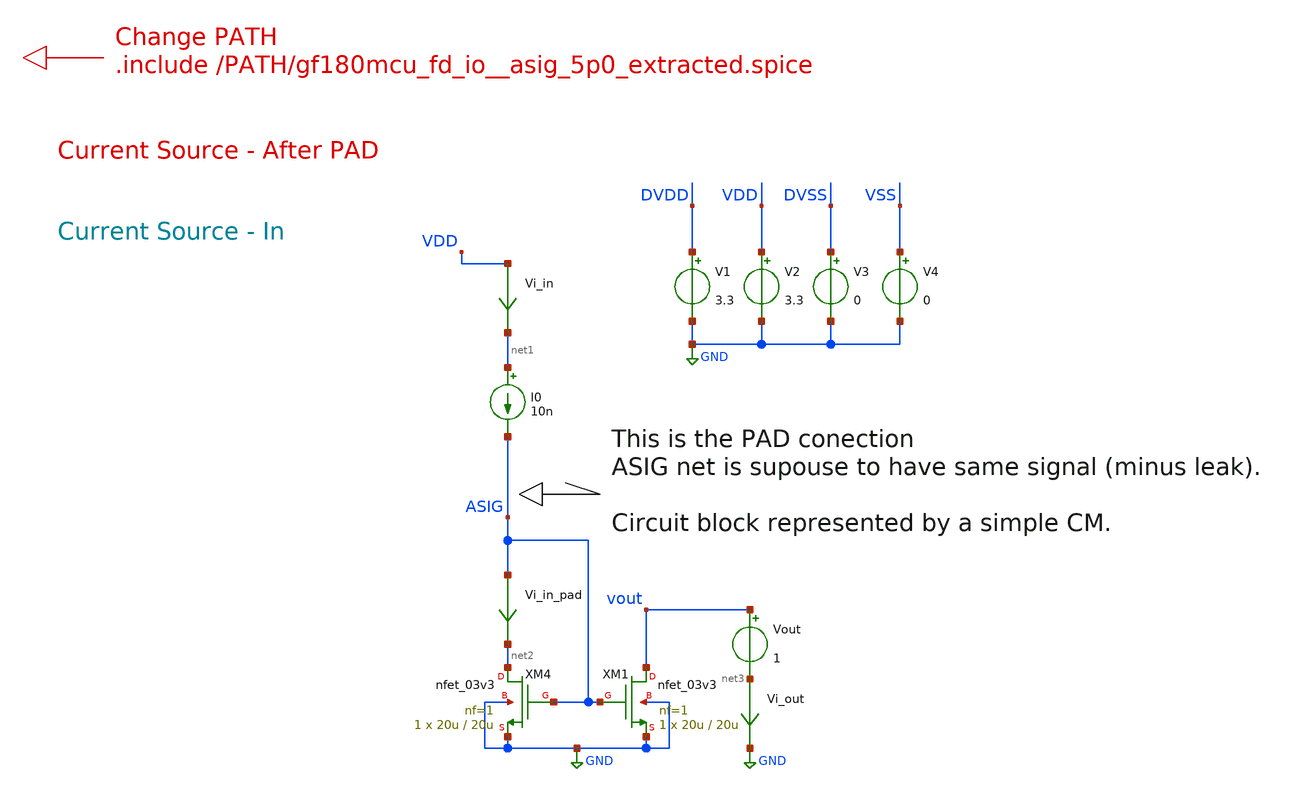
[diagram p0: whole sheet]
** sch_path: designs/Chipathon2025_pads/xschem/analog_leak_pads.sch
**.subckt analog_leak_pads
V1 DVDD GND 3.3
V2 VDD GND 3.3
V3 DVSS GND 0
V4 VSS GND 0
XM1 vout ASIG GND GND nfet_03v3 L=20u W=20u nf=1 ad='int((nf+1)/2) * W/nf * 0.18u' as='int((nf+2)/2) * W/nf * 0.18u'
+ pd='2*int((nf+1)/2) * (W/nf + 0.18u)' ps='2*int((nf+2)/2) * (W/nf + 0.18u)' nrd='0.18u / W' nrs='0.18u / W'
+ sa=0 sb=0 sd=0 m=1
XM4 net2 ASIG GND GND nfet_03v3 L=20u W=20u nf=1 ad='int((nf+1)/2) * W/nf * 0.18u' as='int((nf+2)/2) * W/nf * 0.18u'
+ pd='2*int((nf+1)/2) * (W/nf + 0.18u)' ps='2*int((nf+2)/2) * (W/nf + 0.18u)' nrd='0.18u / W' nrs='0.18u / W'
+ sa=0 sb=0 sd=0 m=1
I0 net1 ASIG 10n
Vi_in VDD net1 0
.save i(vi_in)
Vi_in_pad ASIG net2 0
.save i(vi_in_pad)
Vi_out net3 GND 0
.save i(vi_out)
Vout vout net3 1
**** begin user architecture code


.option gmin=1e-24
.option klu

.control
save all

dc Vout 0 3.3 10m

remzerovec
set filetype = binary
write analog_leak_pads.raw
set appendwrite

.endc



.include $::180MCU_MODELS/design.ngspice
.lib $::180MCU_MODELS/sm141064.ngspice typical
.lib $::180MCU_MODELS/sm141064.ngspice diode_typical
.lib $::180MCU_MODELS/sm141064.ngspice res_typical
.lib $::180MCU_MODELS/sm141064.ngspice mimcap_typical
.lib $::180MCU_MODELS/sm141064.ngspice moscap_typical


.include /home/gmaranhao/Desktop/gf180_work/Pads/gf180mcu_fd_io__asig_5p0_extracted.spice
.include /home/gmaranhao/Desktop/gf180_work/Pads/gf180mcu_fd_io__asig_5p0_gab.spice

*.include /home/gmaranhao/Desktop/gf180_work/Pads/asig5v_io_cell.spice


*Xclosed DVSS DVDD VSS VDD ASIG ASIG gf180mcu_fd_io__asig_5p0_extracted
*Xopen DVSS DVDD ASIG DVDD VSS VDD gf180mcu_fd_io__asig_5p0

Xopen_gab VSS VDD ASIG DVSS DVDD gf180mcu_fd_io__asig_5p0_gab


**** end user architecture code
**.ends
.GLOBAL GND
.end
